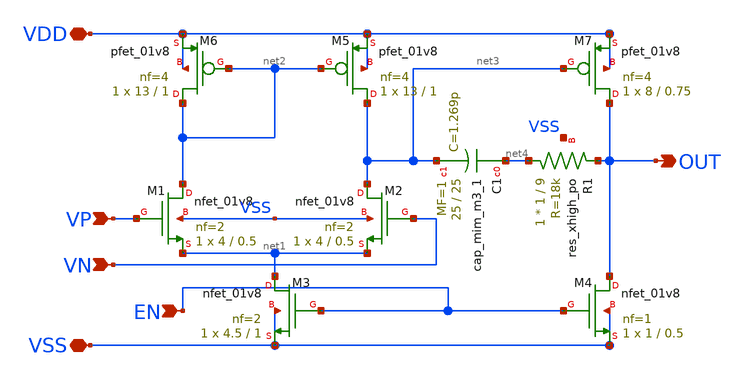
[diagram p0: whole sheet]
** sch_path: LDO_UVLO_Design/LDO2/2-stage-miller.sch
**.subckt 2-stage-miller VSS VDD VP VN OUT EN
*.iopin VSS
*.iopin VDD
*.ipin VP
*.ipin VN
*.opin OUT
*.ipin EN
XM1 net2 VP net1 VSS sky130_fd_pr__nfet_01v8 L=0.5 W=4 nf=2 ad='int((nf+1)/2) * W/nf * 0.29' as='int((nf+2)/2) * W/nf * 0.29'
+ pd='2*int((nf+1)/2) * (W/nf + 0.29)' ps='2*int((nf+2)/2) * (W/nf + 0.29)' nrd='0.29 / W' nrs='0.29 / W'
+ sa=0 sb=0 sd=0 mult=1 m=1
XM2 net3 VN net1 VSS sky130_fd_pr__nfet_01v8 L=0.5 W=4 nf=2 ad='int((nf+1)/2) * W/nf * 0.29' as='int((nf+2)/2) * W/nf * 0.29'
+ pd='2*int((nf+1)/2) * (W/nf + 0.29)' ps='2*int((nf+2)/2) * (W/nf + 0.29)' nrd='0.29 / W' nrs='0.29 / W'
+ sa=0 sb=0 sd=0 mult=1 m=1
XM3 net1 EN VSS VSS sky130_fd_pr__nfet_01v8 L=1 W=4.5 nf=2 ad='int((nf+1)/2) * W/nf * 0.29' as='int((nf+2)/2) * W/nf * 0.29'
+ pd='2*int((nf+1)/2) * (W/nf + 0.29)' ps='2*int((nf+2)/2) * (W/nf + 0.29)' nrd='0.29 / W' nrs='0.29 / W'
+ sa=0 sb=0 sd=0 mult=1 m=1
XM4 OUT EN VSS VSS sky130_fd_pr__nfet_01v8 L=0.5 W=1 nf=1 ad='int((nf+1)/2) * W/nf * 0.29' as='int((nf+2)/2) * W/nf * 0.29'
+ pd='2*int((nf+1)/2) * (W/nf + 0.29)' ps='2*int((nf+2)/2) * (W/nf + 0.29)' nrd='0.29 / W' nrs='0.29 / W'
+ sa=0 sb=0 sd=0 mult=1 m=1
XM5 net3 net2 VDD VDD sky130_fd_pr__pfet_01v8 L=1 W=13 nf=4 ad='int((nf+1)/2) * W/nf * 0.29' as='int((nf+2)/2) * W/nf * 0.29'
+ pd='2*int((nf+1)/2) * (W/nf + 0.29)' ps='2*int((nf+2)/2) * (W/nf + 0.29)' nrd='0.29 / W' nrs='0.29 / W'
+ sa=0 sb=0 sd=0 mult=1 m=1
XM6 net2 net2 VDD VDD sky130_fd_pr__pfet_01v8 L=1 W=13 nf=4 ad='int((nf+1)/2) * W/nf * 0.29' as='int((nf+2)/2) * W/nf * 0.29'
+ pd='2*int((nf+1)/2) * (W/nf + 0.29)' ps='2*int((nf+2)/2) * (W/nf + 0.29)' nrd='0.29 / W' nrs='0.29 / W'
+ sa=0 sb=0 sd=0 mult=1 m=1
XM7 OUT net3 VDD VDD sky130_fd_pr__pfet_01v8 L=0.75 W=8 nf=4 ad='int((nf+1)/2) * W/nf * 0.29' as='int((nf+2)/2) * W/nf * 0.29'
+ pd='2*int((nf+1)/2) * (W/nf + 0.29)' ps='2*int((nf+2)/2) * (W/nf + 0.29)' nrd='0.29 / W' nrs='0.29 / W'
+ sa=0 sb=0 sd=0 mult=1 m=1
XC1 net4 net3 sky130_fd_pr__cap_mim_m3_1 W=25 L=25 MF=1 m=1
XR1 net4 OUT VSS sky130_fd_pr__res_xhigh_po W=1 L=9 mult=1 m=1
**.ends
.end
